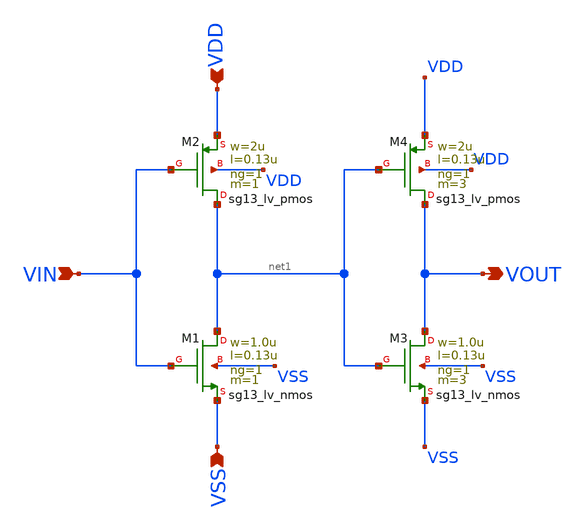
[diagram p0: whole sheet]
** sch_path: work/gate_buff_L0d13/xschem/gate_buff_L0d13.sch
**.subckt gate_buff_L0d13 VDD VIN VSS VOUT
*.ipin VDD
*.ipin VIN
*.ipin VSS
*.opin VOUT
XM1 net1 VIN VSS VSS sg13_lv_nmos w=1.0u l=0.13u ng=1 m=1 mm_ok=1
XM2 net1 VIN VDD VDD sg13_lv_pmos w=2u l=0.13u ng=1 m=1 mm_ok=1
XM3 VOUT net1 VSS VSS sg13_lv_nmos w=1.0u l=0.13u ng=1 m=3 mm_ok=1
XM4 VOUT net1 VDD VDD sg13_lv_pmos w=2u l=0.13u ng=1 m=3 mm_ok=1
**.ends
.end
